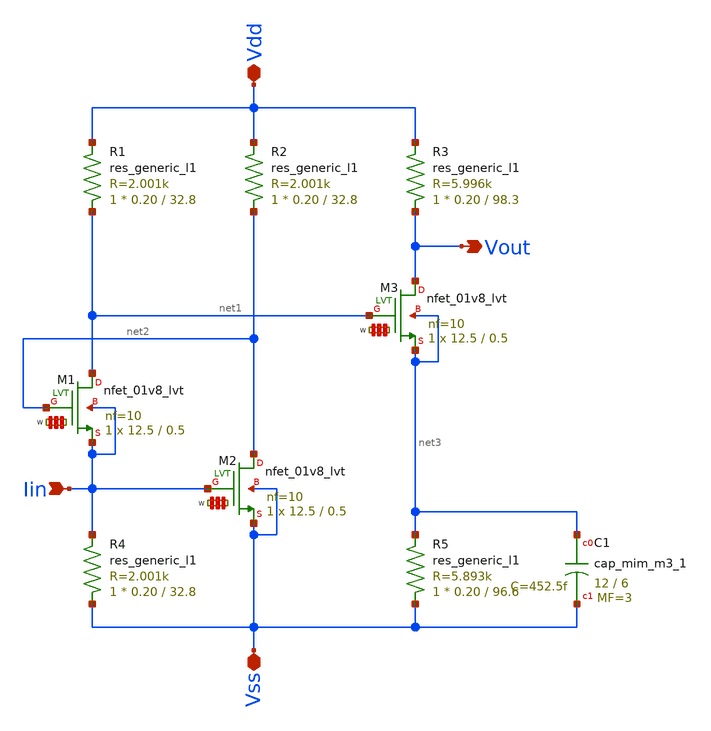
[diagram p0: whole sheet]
** sch_path: analog/library/TIAs/RGC-TIA/Transamp.sch
**.subckt Transamp Iin Vout Vss Vdd
*.ipin Iin
*.opin Vout
*.iopin Vss
*.iopin Vdd
R1 net1 Vdd sky130_fd_pr__res_generic_l1 W=0.20 L=32.8 m=1
R2 net2 Vdd sky130_fd_pr__res_generic_l1 W=0.20 L=32.8 m=1
R4 Vss Iin sky130_fd_pr__res_generic_l1 W=0.20 L=32.8 m=1
XM1 net1 net2 Iin Iin sky130_fd_pr__nfet_01v8_lvt L=0.5 W='12.5 * 10 ' nf=10 ad='int((10 + 1)/2) * 12.5 / 10 * 0.29'
+ as='int((10 + 2)/2) * 12.5 / 10 * 0.29' pd='2*int((10 + 1)/2) * (12.5 / 10 + 0.29)' ps='2*int((10 + 2)/2) * (12.5 / 10 + 0.29)'
+ nrd='0.29 / 12.5 ' nrs='0.29 / 12.5 ' sa=0 sb=0 sd=0 mult=1 m=1
XM2 net2 Iin Vss Vss sky130_fd_pr__nfet_01v8_lvt L=0.5 W='12.5 * 10 ' nf=10 ad='int((10 + 1)/2) * 12.5 / 10 * 0.29'
+ as='int((10 + 2)/2) * 12.5 / 10 * 0.29' pd='2*int((10 + 1)/2) * (12.5 / 10 + 0.29)' ps='2*int((10 + 2)/2) * (12.5 / 10 + 0.29)'
+ nrd='0.29 / 12.5 ' nrs='0.29 / 12.5 ' sa=0 sb=0 sd=0 mult=1 m=1
R3 Vout Vdd sky130_fd_pr__res_generic_l1 W=0.20 L=98.3 m=1
XM3 Vout net1 net3 net3 sky130_fd_pr__nfet_01v8_lvt L=0.5 W='12.5 * 10 ' nf=10 ad='int((10 + 1)/2) * 12.5 / 10 * 0.29'
+ as='int((10 + 2)/2) * 12.5 / 10 * 0.29' pd='2*int((10 + 1)/2) * (12.5 / 10 + 0.29)' ps='2*int((10 + 2)/2) * (12.5 / 10 + 0.29)'
+ nrd='0.29 / 12.5 ' nrs='0.29 / 12.5 ' sa=0 sb=0 sd=0 mult=1 m=1
R5 Vss net3 sky130_fd_pr__res_generic_l1 W=0.20 L=96.6 m=1
XC1 net3 Vss sky130_fd_pr__cap_mim_m3_1 W=12 L=6 MF=3 m=3
**.ends
.end
